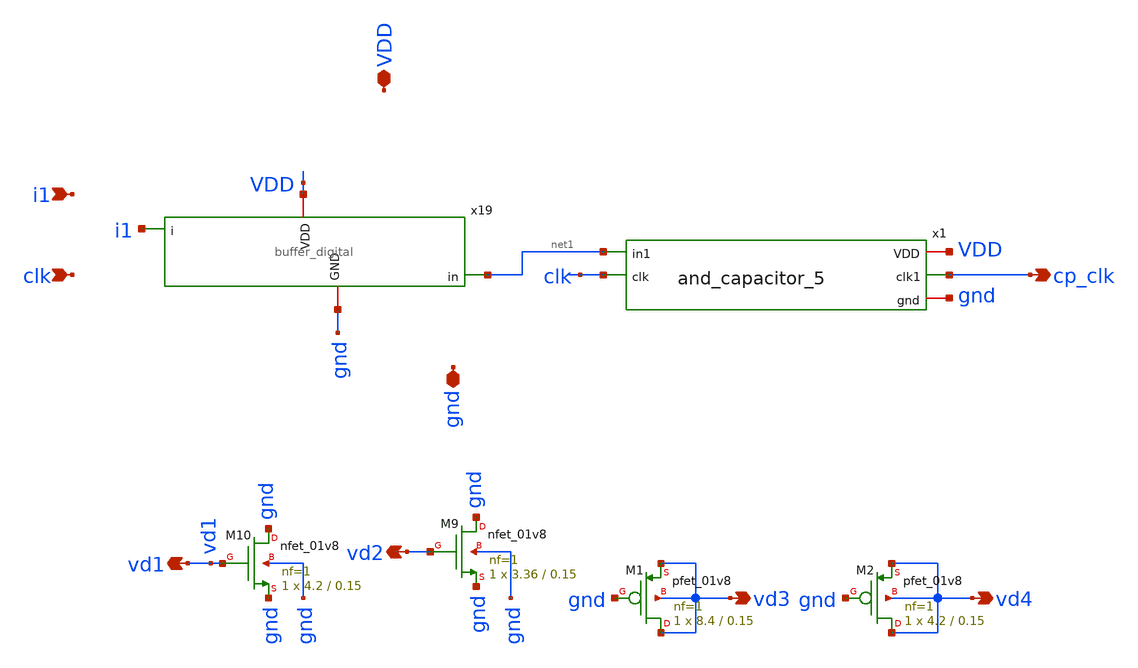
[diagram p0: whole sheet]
** sch_path: xschem/capacitor_5.sch
**.subckt capacitor_5 i1 clk cp_clk VDD gnd vd1 vd2 vd3 vd4
*.ipin i1
*.ipin clk
*.opin cp_clk
*.iopin VDD
*.iopin gnd
*.opin vd1
*.opin vd2
*.opin vd3
*.opin vd4
x19 gnd VDD i1 net1 buffer_digital
x1 net1 VDD clk cp_clk gnd and_capacitor_5
XM9 gnd vd2 gnd gnd sky130_fd_pr__nfet_01v8 L=0.15 W=3.36 nf=1 ad='int((nf+1)/2) * W/nf * 0.29' as='int((nf+2)/2) * W/nf * 0.29'
+ pd='2*int((nf+1)/2) * (W/nf + 0.29)' ps='2*int((nf+2)/2) * (W/nf + 0.29)' nrd='0.29 / W' nrs='0.29 / W'
+ sa=0 sb=0 sd=0 mult=1 m=1
XM10 gnd vd1 gnd gnd sky130_fd_pr__nfet_01v8 L=0.15 W=4.2 nf=1 ad='int((nf+1)/2) * W/nf * 0.29' as='int((nf+2)/2) * W/nf * 0.29'
+ pd='2*int((nf+1)/2) * (W/nf + 0.29)' ps='2*int((nf+2)/2) * (W/nf + 0.29)' nrd='0.29 / W' nrs='0.29 / W'
+ sa=0 sb=0 sd=0 mult=1 m=1
XM1 vd3 gnd vd3 vd3 sky130_fd_pr__pfet_01v8 L=0.15 W=8.4 nf=1 ad='int((nf+1)/2) * W/nf * 0.29' as='int((nf+2)/2) * W/nf * 0.29'
+ pd='2*int((nf+1)/2) * (W/nf + 0.29)' ps='2*int((nf+2)/2) * (W/nf + 0.29)' nrd='0.29 / W' nrs='0.29 / W'
+ sa=0 sb=0 sd=0 mult=1 m=1
XM2 vd4 gnd vd4 vd4 sky130_fd_pr__pfet_01v8 L=0.15 W=4.2 nf=1 ad='int((nf+1)/2) * W/nf * 0.29' as='int((nf+2)/2) * W/nf * 0.29'
+ pd='2*int((nf+1)/2) * (W/nf + 0.29)' ps='2*int((nf+2)/2) * (W/nf + 0.29)' nrd='0.29 / W' nrs='0.29 / W'
+ sa=0 sb=0 sd=0 mult=1 m=1
**.ends
.end
